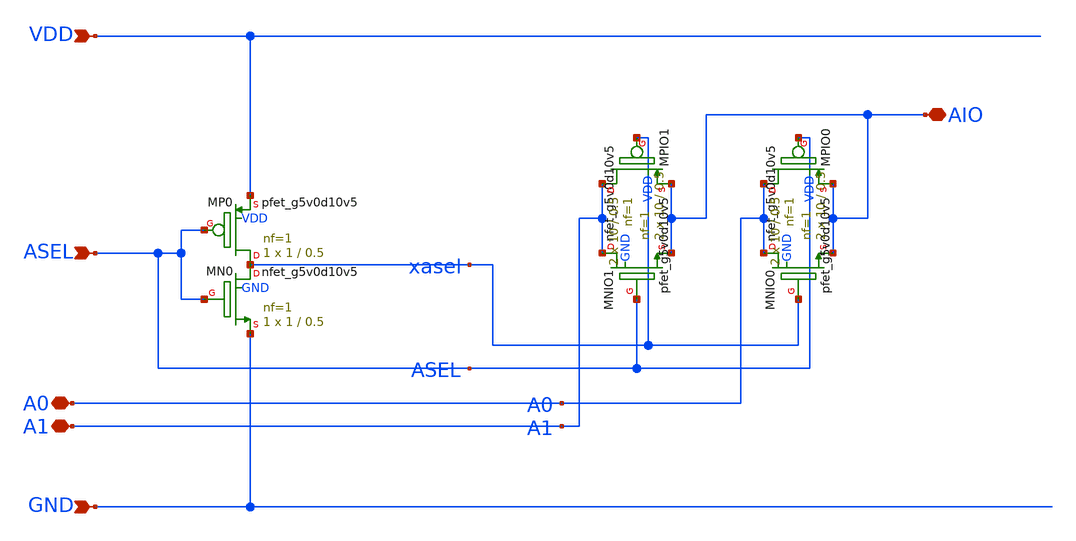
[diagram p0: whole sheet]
** sch_path: design/schematic/mux3V3_v1.sch
**.subckt mux3V3_v1 VDD AIO ASEL A0 A1 GND
*.ipin VDD
*.iopin AIO
*.ipin ASEL
*.iopin A0
*.iopin A1
*.ipin GND
XMNIO0 A0 xasel AIO GND sky130_fd_pr__nfet_g5v0d10v5 L=0.5 W=10 nf=1 ad='int((nf+1)/2) * W/nf * 0.29'
+ as='int((nf+2)/2) * W/nf * 0.29' pd='2*int((nf+1)/2) * (W/nf + 0.29)' ps='2*int((nf+2)/2) * (W/nf + 0.29)'
+ nrd='0.29 / W' nrs='0.29 / W' sa=0 sb=0 sd=0 mult=2 m=2
XMPIO0 A0 ASEL AIO VDD sky130_fd_pr__pfet_g5v0d10v5 L=0.5 W=10 nf=1 ad='int((nf+1)/2) * W/nf * 0.29'
+ as='int((nf+2)/2) * W/nf * 0.29' pd='2*int((nf+1)/2) * (W/nf + 0.29)' ps='2*int((nf+2)/2) * (W/nf + 0.29)'
+ nrd='0.29 / W' nrs='0.29 / W' sa=0 sb=0 sd=0 mult=2 m=2
XMNIO1 A1 ASEL AIO GND sky130_fd_pr__nfet_g5v0d10v5 L=0.5 W=10 nf=1 ad='int((nf+1)/2) * W/nf * 0.29'
+ as='int((nf+2)/2) * W/nf * 0.29' pd='2*int((nf+1)/2) * (W/nf + 0.29)' ps='2*int((nf+2)/2) * (W/nf + 0.29)'
+ nrd='0.29 / W' nrs='0.29 / W' sa=0 sb=0 sd=0 mult=2 m=2
XMPIO1 A1 xasel AIO VDD sky130_fd_pr__pfet_g5v0d10v5 L=0.5 W=10 nf=1 ad='int((nf+1)/2) * W/nf * 0.29'
+ as='int((nf+2)/2) * W/nf * 0.29' pd='2*int((nf+1)/2) * (W/nf + 0.29)' ps='2*int((nf+2)/2) * (W/nf + 0.29)'
+ nrd='0.29 / W' nrs='0.29 / W' sa=0 sb=0 sd=0 mult=2 m=2
XMP0 xasel ASEL VDD VDD sky130_fd_pr__pfet_g5v0d10v5 L=0.5 W=1 nf=1 ad='int((nf+1)/2) * W/nf * 0.29'
+ as='int((nf+2)/2) * W/nf * 0.29' pd='2*int((nf+1)/2) * (W/nf + 0.29)' ps='2*int((nf+2)/2) * (W/nf + 0.29)'
+ nrd='0.29 / W' nrs='0.29 / W' sa=0 sb=0 sd=0 mult=1 m=1
XMN0 xasel ASEL GND GND sky130_fd_pr__nfet_g5v0d10v5 L=0.5 W=1 nf=1 ad='int((nf+1)/2) * W/nf * 0.29'
+ as='int((nf+2)/2) * W/nf * 0.29' pd='2*int((nf+1)/2) * (W/nf + 0.29)' ps='2*int((nf+2)/2) * (W/nf + 0.29)'
+ nrd='0.29 / W' nrs='0.29 / W' sa=0 sb=0 sd=0 mult=1 m=1
**.ends
.end
